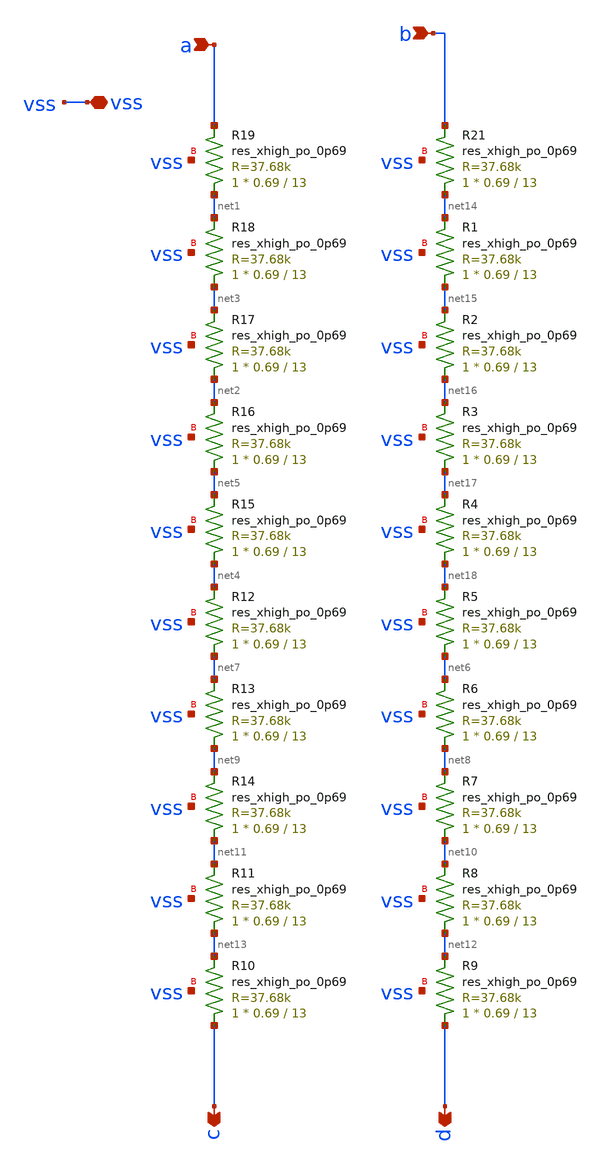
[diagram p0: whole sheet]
** sch_path: schematic/bandgapxd/bg_res.sch
**.subckt bg_res vss a b c d
*.iopin vss
*.ipin a
*.ipin b
*.opin c
*.opin d
XR21 net14 b vss sky130_fd_pr__res_xhigh_po_0p69 L=13 mult=1 m=1
XR1 net15 net14 vss sky130_fd_pr__res_xhigh_po_0p69 L=13 mult=1 m=1
XR2 net16 net15 vss sky130_fd_pr__res_xhigh_po_0p69 L=13 mult=1 m=1
XR3 net17 net16 vss sky130_fd_pr__res_xhigh_po_0p69 L=13 mult=1 m=1
XR4 net18 net17 vss sky130_fd_pr__res_xhigh_po_0p69 L=13 mult=1 m=1
XR5 net6 net18 vss sky130_fd_pr__res_xhigh_po_0p69 L=13 mult=1 m=1
XR6 net8 net6 vss sky130_fd_pr__res_xhigh_po_0p69 L=13 mult=1 m=1
XR7 net10 net8 vss sky130_fd_pr__res_xhigh_po_0p69 L=13 mult=1 m=1
XR8 net12 net10 vss sky130_fd_pr__res_xhigh_po_0p69 L=13 mult=1 m=1
XR9 d net12 vss sky130_fd_pr__res_xhigh_po_0p69 L=13 mult=1 m=1
XR10 c net13 vss sky130_fd_pr__res_xhigh_po_0p69 L=13 mult=1 m=1
XR11 net13 net11 vss sky130_fd_pr__res_xhigh_po_0p69 L=13 mult=1 m=1
XR12 net7 net4 vss sky130_fd_pr__res_xhigh_po_0p69 L=13 mult=1 m=1
XR13 net9 net7 vss sky130_fd_pr__res_xhigh_po_0p69 L=13 mult=1 m=1
XR14 net11 net9 vss sky130_fd_pr__res_xhigh_po_0p69 L=13 mult=1 m=1
XR15 net4 net5 vss sky130_fd_pr__res_xhigh_po_0p69 L=13 mult=1 m=1
XR16 net5 net2 vss sky130_fd_pr__res_xhigh_po_0p69 L=13 mult=1 m=1
XR17 net2 net3 vss sky130_fd_pr__res_xhigh_po_0p69 L=13 mult=1 m=1
XR18 net3 net1 vss sky130_fd_pr__res_xhigh_po_0p69 L=13 mult=1 m=1
XR19 net1 a vss sky130_fd_pr__res_xhigh_po_0p69 L=13 mult=1 m=1
**.ends
.end
